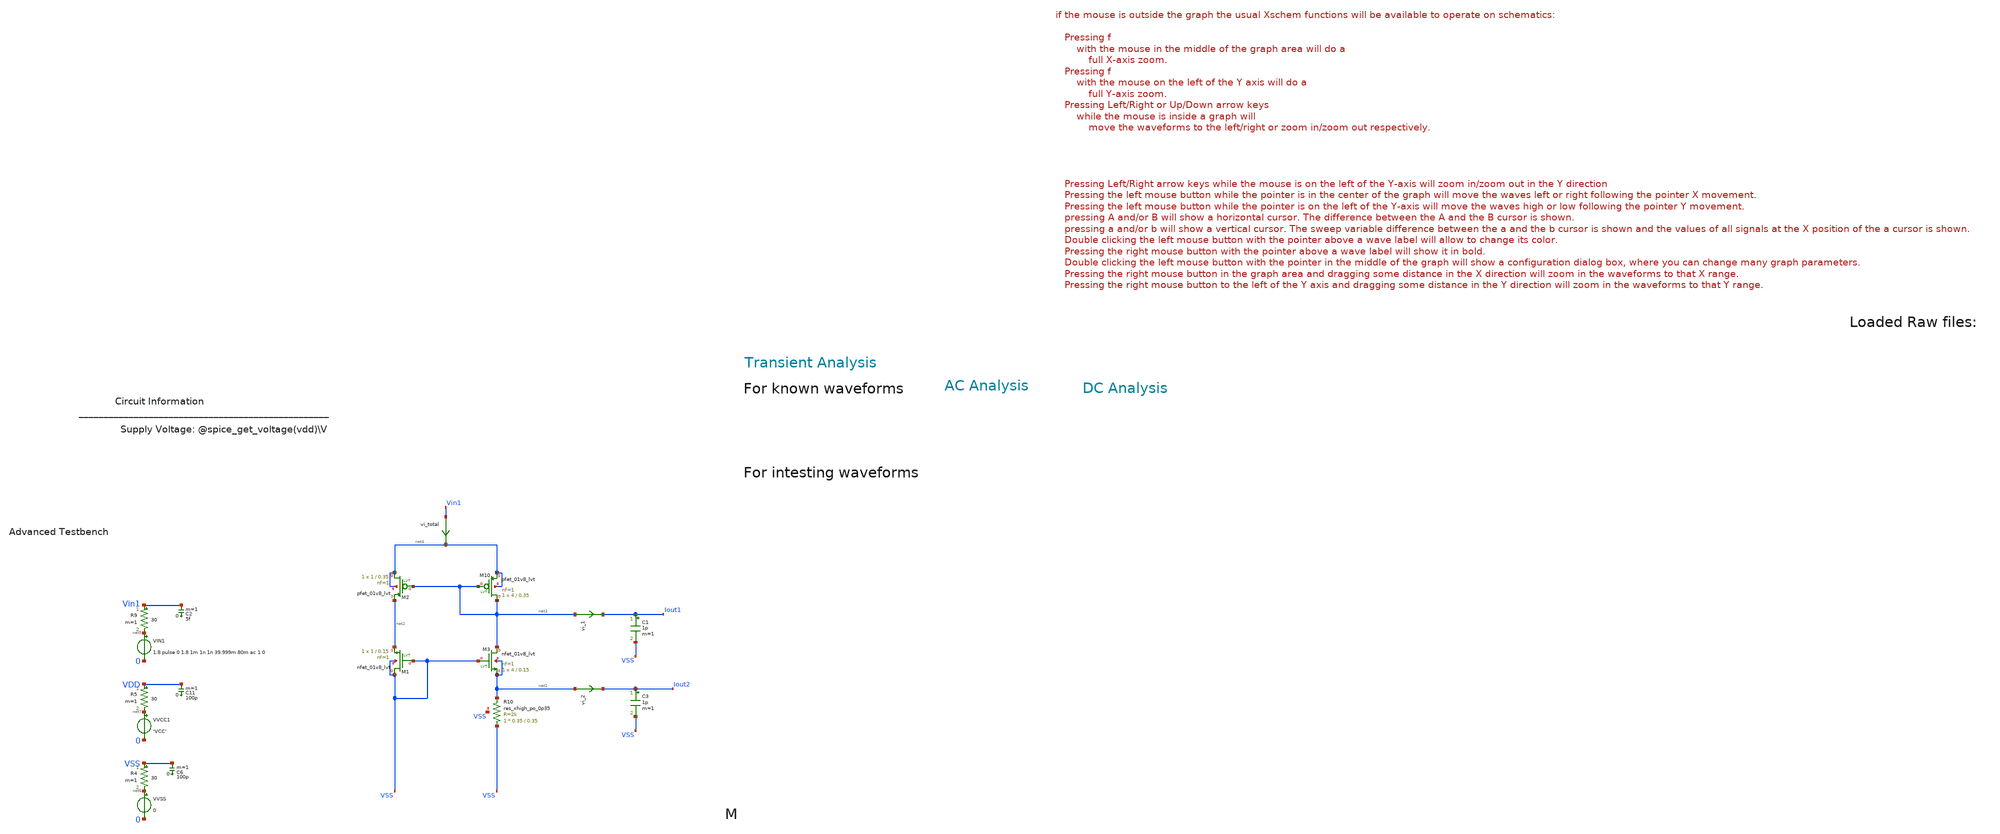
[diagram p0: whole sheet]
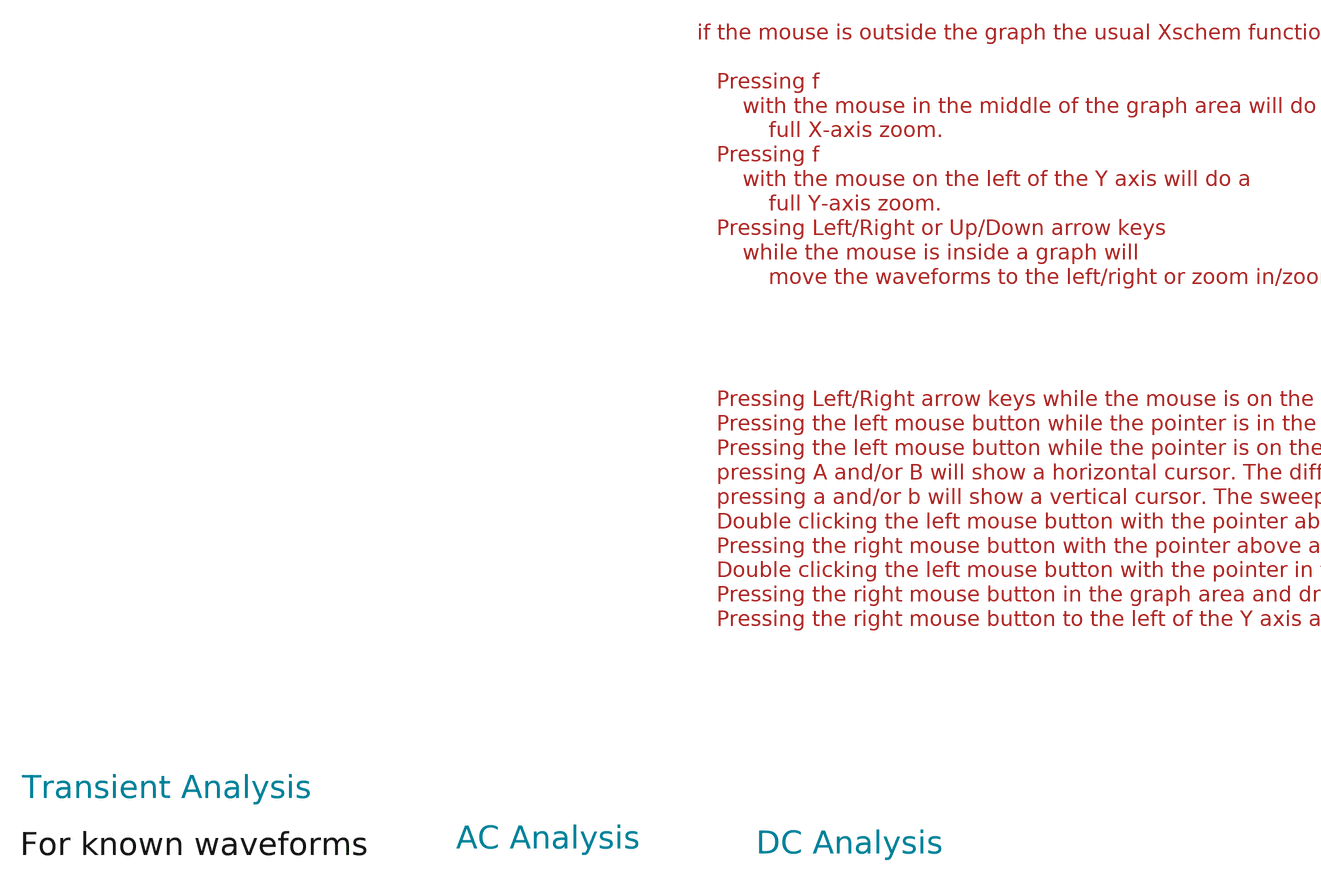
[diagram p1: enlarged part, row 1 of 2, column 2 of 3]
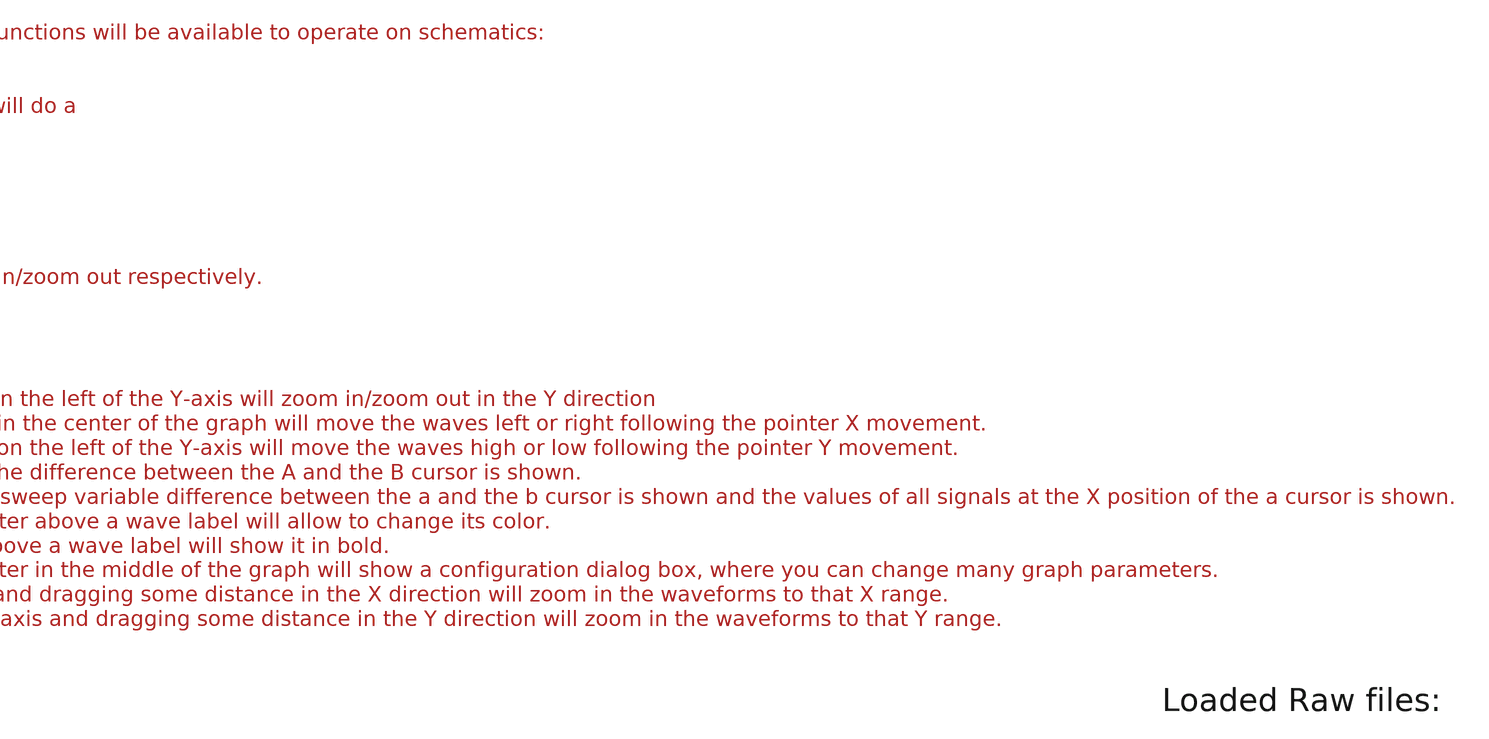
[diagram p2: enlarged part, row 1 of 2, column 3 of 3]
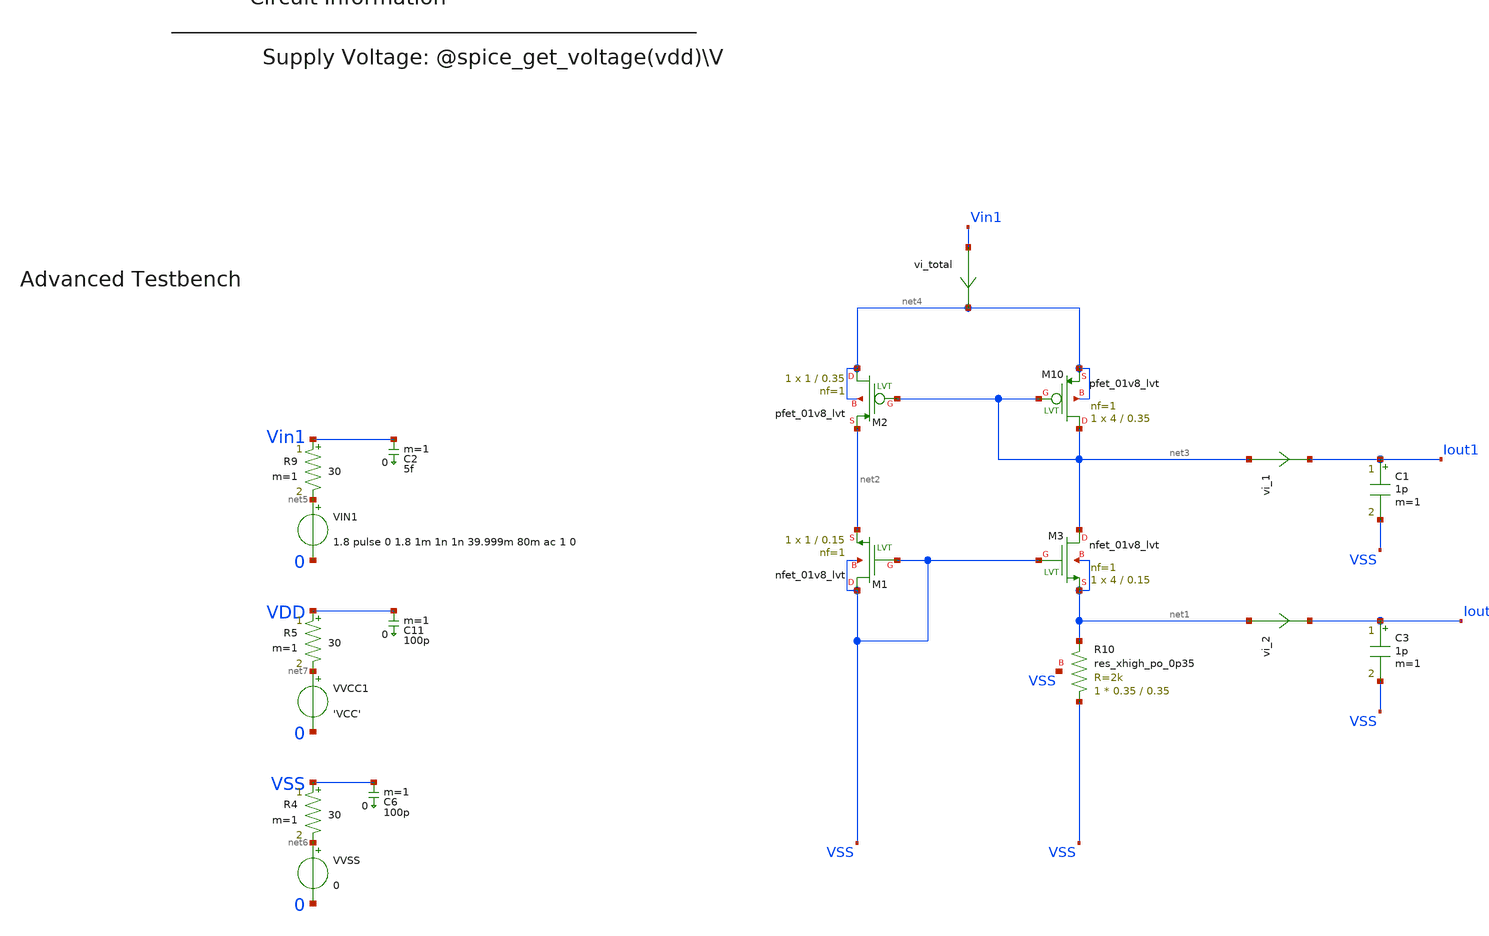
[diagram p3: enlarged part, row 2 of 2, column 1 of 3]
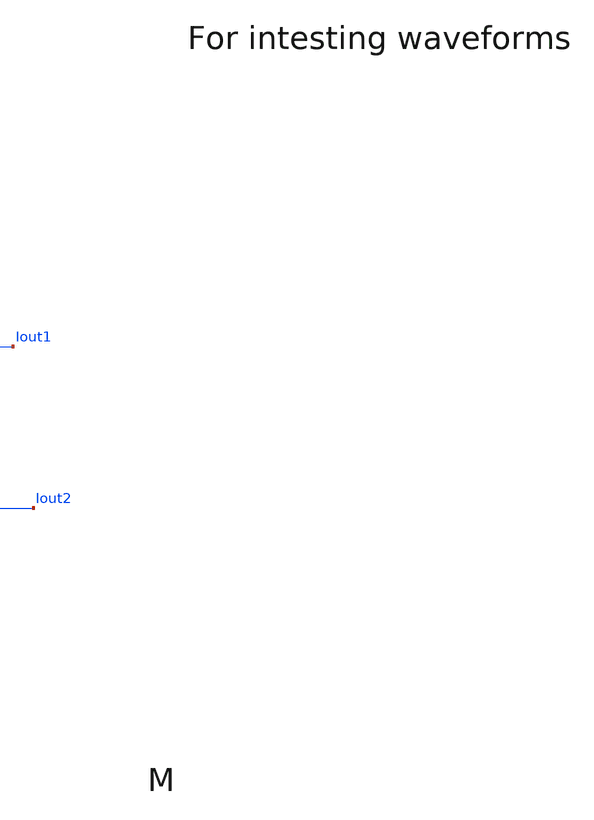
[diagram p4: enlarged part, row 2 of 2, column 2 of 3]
** sch_path: tt10-hdl/tt_um_test_commit/xschem/T0/currMirr/curr_mirror_tb2.sch
* Copyright (C) 1998-2024 Stefan Frederik Schippers
* This program is free software; you can redistribute it and/or modify
* it under the terms of the GNU General Public License as published by
* the Free Software Foundation; either version 2 of the License, or
* (at your option) any later version.
* This program is distributed in the hope that it will be useful,
* but WITHOUT ANY WARRANTY; without even the implied warranty of
* MERCHANTABILITY or FITNESS FOR A PARTICULAR PURPOSE.  See the
* GNU General Public License for more details.
* You should have received a copy of the GNU General Public License
* along with this program; if not, write to the Free Software
**.subckt curr_mirror_tb2
VIN1 net5 0 1.8 pulse 0 1.8 1m 1n 1n 39.999m 80m ac 1 0
VVSS net6 0 0
R4 VSS net6 30 m=1
C6 VSS 0 100p m=1
VVCC1 net7 0 'VCC'
R5 VDD net7 30 m=1
C11 VDD 0 100p m=1
R9 Vin1 net5 30 m=1
C2 Vin1 0 5f m=1
XM10 net3 net3 net4 net4 sky130_fd_pr__pfet_01v8_lvt L=0.35 W=4 nf=1 ad='int((1 + 1)/2) * 4 / 1 * 0.29'
+ as='int((1 + 2)/2) * 4 / 1 * 0.29' pd='2*int((1 + 1)/2) * (4 / 1 + 0.29)' ps='2*int((1 + 2)/2) * (4 / 1 + 0.29)'
+ nrd='0.29 / 4 ' nrs='0.29 / 4 ' sa=0 sb=0 sd=0 mult=1 m=1
XM1 VSS VSS net2 VSS sky130_fd_pr__nfet_01v8_lvt L=0.15 W=1 nf=1 ad='int((1 + 1)/2) * 1 / 1 * 0.29' as='int((1 + 2)/2) * 1 / 1 * 0.29'
+ pd='2*int((1 + 1)/2) * (1 / 1 + 0.29)' ps='2*int((1 + 2)/2) * (1 / 1 + 0.29)' nrd='0.29 / 1 ' nrs='0.29 / 1 '
+ sa=0 sb=0 sd=0 mult=1 m=1
XR10 VSS net1 VSS sky130_fd_pr__res_xhigh_po_0p35 L=0.35 mult=1 m=1
XM2 net4 net3 net2 net4 sky130_fd_pr__pfet_01v8_lvt L=0.35 W=1 nf=1 ad='int((1 + 1)/2) * 1 / 1 * 0.29'
+ as='int((1 + 2)/2) * 1 / 1 * 0.29' pd='2*int((1 + 1)/2) * (1 / 1 + 0.29)' ps='2*int((1 + 2)/2) * (1 / 1 + 0.29)'
+ nrd='0.29 / 1 ' nrs='0.29 / 1 ' sa=0 sb=0 sd=0 mult=1 m=1
XM3 net3 VSS net1 net1 sky130_fd_pr__nfet_01v8_lvt L=0.15 W=4 nf=1 ad='int((1 + 1)/2) * 4 / 1 * 0.29'
+ as='int((1 + 2)/2) * 4 / 1 * 0.29' pd='2*int((1 + 1)/2) * (4 / 1 + 0.29)' ps='2*int((1 + 2)/2) * (4 / 1 + 0.29)'
+ nrd='0.29 / 4 ' nrs='0.29 / 4 ' sa=0 sb=0 sd=0 mult=1 m=1
vi_1 net3 Iout1 0
.save i(vi_1)
vi_2 net1 Iout2 0
.save i(vi_2)
vi_total Vin1 net4 0
.save i(vi_total)
C1 Iout1 VSS 1p m=1
C3 Iout2 VSS 1p m=1
**** begin user architecture code



.temp 30
*.param IB=1n
.param VCC = 1.8

.option savecurrents
.save all @m1[gm]
.control
  save all alli
  op
  let power=-v(vcc) * i(vvcc)
  settype power power
  write template_adv_tb.raw
  set appendwrite

  *dc vin1 0 1.8 0.001
  *write template_adv_tb.raw

  tran 0.5m  500m
  *tran 0.01n 15n
  write template_adv_tb.raw

  *ac dec 10 1 1G
  *remzerovec
  *write template_adv_tb.raw



  quit 0




.endc





** opencircuitdesign pdks install
.lib $::SKYWATER_MODELS/sky130.lib.spice tt
.include $::SKYWATER_STDCELLS/sky130_fd_sc_hd.spice


**** end user architecture code
**.ends
.end
